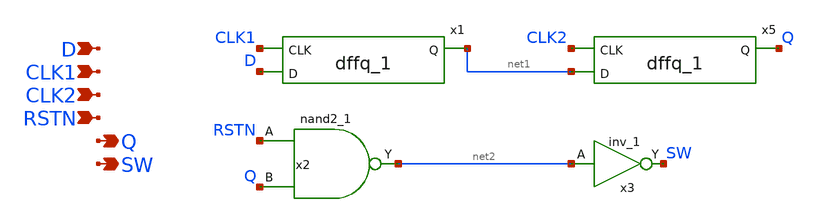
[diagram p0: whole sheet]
** sch_path: designs/libs/core_switch-matrix/dff_2_phase/dff_2_phase.sch
**.subckt dff_2_phase CLK1 D RSTN CLK2 SW Q
*.ipin CLK1
*.ipin D
*.ipin RSTN
*.ipin CLK2
*.opin SW
*.opin Q
x1 D CLK1 net1 VDDd VDDd VSSd VSSd gf180mcu_fd_sc_mcu9t5v0__dffq_1
x5 net1 CLK2 Q VDDd VDDd VSSd VSSd gf180mcu_fd_sc_mcu9t5v0__dffq_1
x2 RSTN Q VSSd VDDd VSSd VDDd net2 gf180mcu_fd_sc_mcu9t5v0__nand2_1
x3 net2 VSSd VDDd VSSd VDDd SW gf180mcu_fd_sc_mcu9t5v0__inv_1
**.ends
.end
